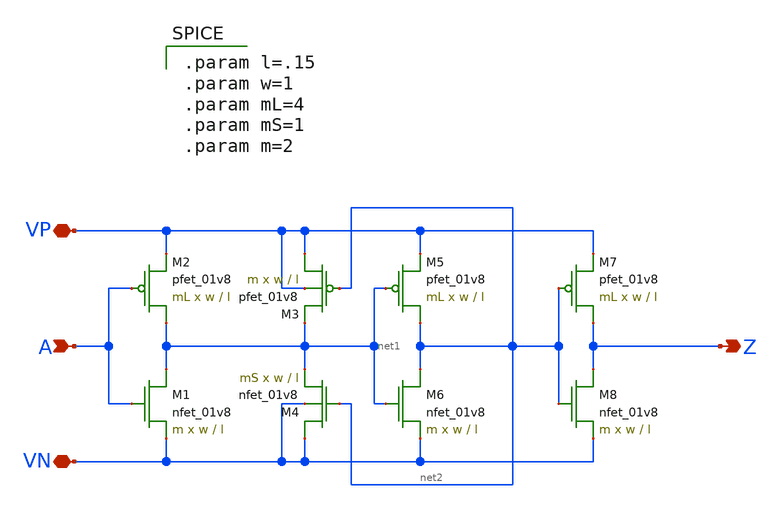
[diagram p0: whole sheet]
** sch_path: schematics/inverterSchmitt.sch
**.subckt inverterSchmitt A VP VN Z
*.ipin A
*.iopin VP
*.iopin VN
*.opin Z
XM1 net1 A VN GND sky130_fd_pr__nfet_01v8 L=l W=w nf=1 ad='int((nf+1)/2) * W/nf * 0.29' as='int((nf+2)/2) * W/nf * 0.29'
+ pd='2*int((nf+1)/2) * (W/nf + 0.29)' ps='2*int((nf+2)/2) * (W/nf + 0.29)' nrd='0.29 / W' nrs='0.29 / W'
+ sa=0 sb=0 sd=0 mult=m m=m
XM2 net1 A VP VDD sky130_fd_pr__pfet_01v8 L=l W=w nf=1 ad='int((nf+1)/2) * W/nf * 0.29' as='int((nf+2)/2) * W/nf * 0.29'
+ pd='2*int((nf+1)/2) * (W/nf + 0.29)' ps='2*int((nf+2)/2) * (W/nf + 0.29)' nrd='0.29 / W' nrs='0.29 / W'
+ sa=0 sb=0 sd=0 mult=mL m=mL
XM5 net2 net1 VP VDD sky130_fd_pr__pfet_01v8 L=l W=w nf=1 ad='int((nf+1)/2) * W/nf * 0.29' as='int((nf+2)/2) * W/nf * 0.29'
+ pd='2*int((nf+1)/2) * (W/nf + 0.29)' ps='2*int((nf+2)/2) * (W/nf + 0.29)' nrd='0.29 / W' nrs='0.29 / W'
+ sa=0 sb=0 sd=0 mult=mL m=mL
XM6 net2 net1 VN GND sky130_fd_pr__nfet_01v8 L=l W=w nf=1 ad='int((nf+1)/2) * W/nf * 0.29' as='int((nf+2)/2) * W/nf * 0.29'
+ pd='2*int((nf+1)/2) * (W/nf + 0.29)' ps='2*int((nf+2)/2) * (W/nf + 0.29)' nrd='0.29 / W' nrs='0.29 / W'
+ sa=0 sb=0 sd=0 mult=m m=m
XM3 VP net2 net1 VP sky130_fd_pr__pfet_01v8 L=l W=w nf=1 ad='int((nf+1)/2) * W/nf * 0.29' as='int((nf+2)/2) * W/nf * 0.29'
+ pd='2*int((nf+1)/2) * (W/nf + 0.29)' ps='2*int((nf+2)/2) * (W/nf + 0.29)' nrd='0.29 / W' nrs='0.29 / W'
+ sa=0 sb=0 sd=0 mult=m m=m
XM4 VN net2 net1 VN sky130_fd_pr__nfet_01v8 L=l W=w nf=1 ad='int((nf+1)/2) * W/nf * 0.29' as='int((nf+2)/2) * W/nf * 0.29'
+ pd='2*int((nf+1)/2) * (W/nf + 0.29)' ps='2*int((nf+2)/2) * (W/nf + 0.29)' nrd='0.29 / W' nrs='0.29 / W'
+ sa=0 sb=0 sd=0 mult=mS m=mS
XM7 Z net2 VP VDD sky130_fd_pr__pfet_01v8 L=l W=w nf=1 ad='int((nf+1)/2) * W/nf * 0.29' as='int((nf+2)/2) * W/nf * 0.29'
+ pd='2*int((nf+1)/2) * (W/nf + 0.29)' ps='2*int((nf+2)/2) * (W/nf + 0.29)' nrd='0.29 / W' nrs='0.29 / W'
+ sa=0 sb=0 sd=0 mult=mL m=mL
XM8 Z net2 VN GND sky130_fd_pr__nfet_01v8 L=l W=w nf=1 ad='int((nf+1)/2) * W/nf * 0.29' as='int((nf+2)/2) * W/nf * 0.29'
+ pd='2*int((nf+1)/2) * (W/nf + 0.29)' ps='2*int((nf+2)/2) * (W/nf + 0.29)' nrd='0.29 / W' nrs='0.29 / W'
+ sa=0 sb=0 sd=0 mult=m m=m
**** begin user architecture code

.param l=.15
.param w=1
.param mL=4
.param mS=1
.param m=2

**** end user architecture code
**.ends
.end
